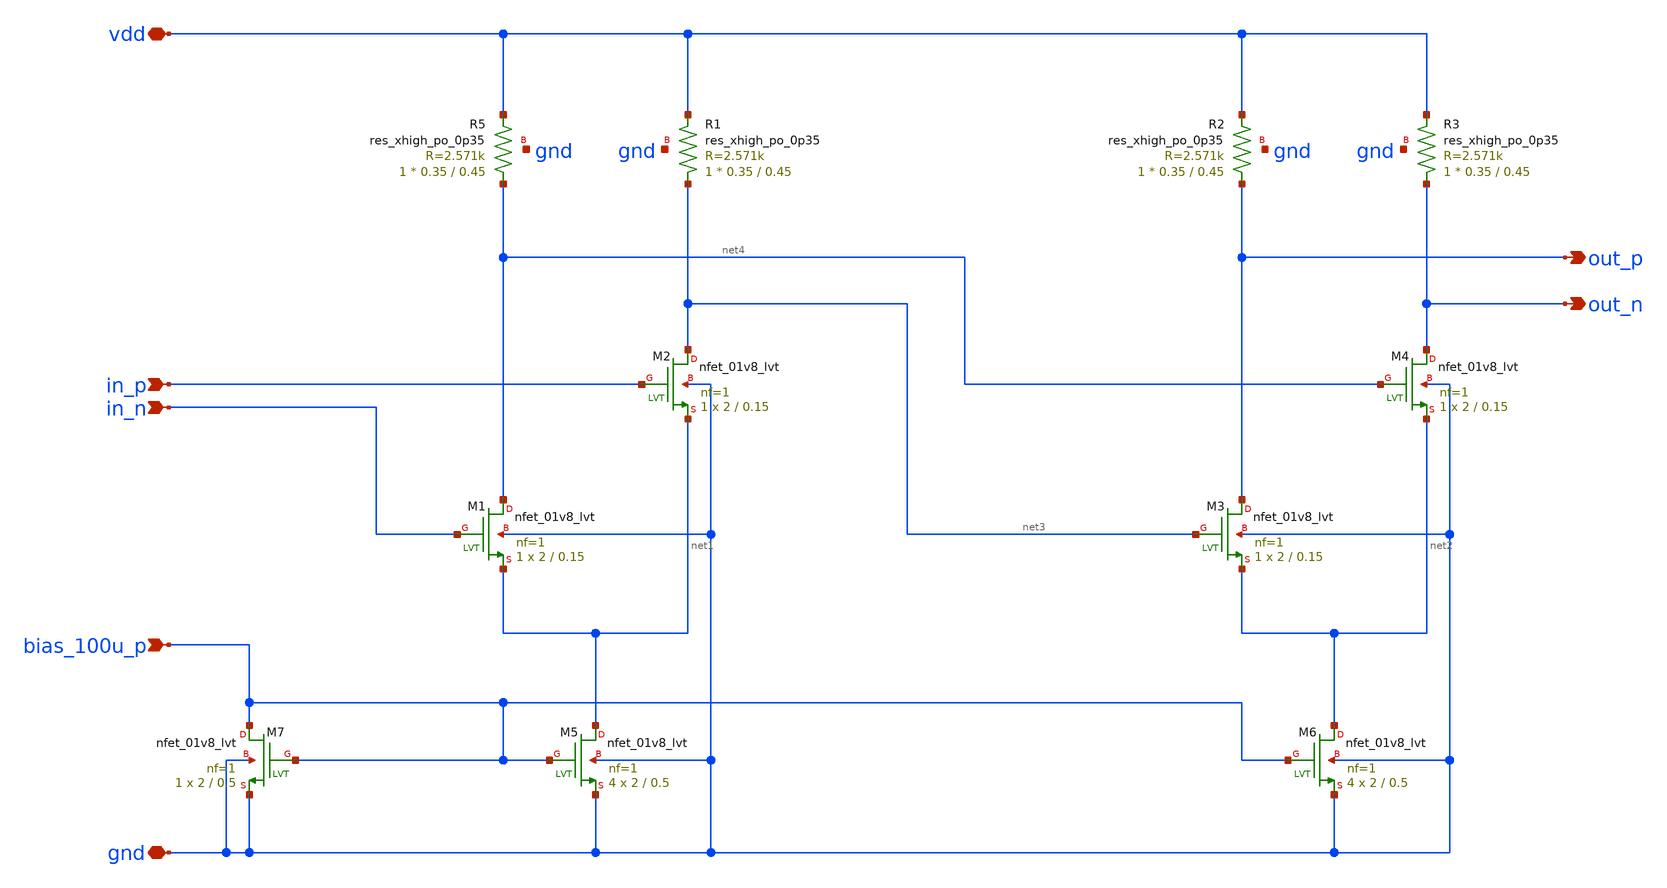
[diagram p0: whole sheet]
** sch_path: design/lc_oscillator_buffer/lc_oscillator_buffer.sch
**.subckt lc_oscillator_buffer gnd vdd out_p out_n bias_100u_p in_p in_n
*.iopin gnd
*.iopin vdd
*.opin out_p
*.opin out_n
*.ipin bias_100u_p
*.ipin in_p
*.ipin in_n
XM1 net4 in_n net1 gnd sky130_fd_pr__nfet_01v8_lvt L=0.15 W=2 nf=1 ad='int((nf+1)/2) * W/nf * 0.29' as='int((nf+2)/2) * W/nf * 0.29'
+ pd='2*int((nf+1)/2) * (W/nf + 0.29)' ps='2*int((nf+2)/2) * (W/nf + 0.29)' nrd='0.29 / W' nrs='0.29 / W'
+ sa=0 sb=0 sd=0 mult=1 m=1
XM2 net3 in_p net1 gnd sky130_fd_pr__nfet_01v8_lvt L=0.15 W=2 nf=1 ad='int((nf+1)/2) * W/nf * 0.29' as='int((nf+2)/2) * W/nf * 0.29'
+ pd='2*int((nf+1)/2) * (W/nf + 0.29)' ps='2*int((nf+2)/2) * (W/nf + 0.29)' nrd='0.29 / W' nrs='0.29 / W'
+ sa=0 sb=0 sd=0 mult=1 m=1
XM3 out_p net3 net2 gnd sky130_fd_pr__nfet_01v8_lvt L=0.15 W=2 nf=1 ad='int((nf+1)/2) * W/nf * 0.29'
+ as='int((nf+2)/2) * W/nf * 0.29' pd='2*int((nf+1)/2) * (W/nf + 0.29)' ps='2*int((nf+2)/2) * (W/nf + 0.29)'
+ nrd='0.29 / W' nrs='0.29 / W' sa=0 sb=0 sd=0 mult=1 m=1
XM4 out_n net4 net2 gnd sky130_fd_pr__nfet_01v8_lvt L=0.15 W=2 nf=1 ad='int((nf+1)/2) * W/nf * 0.29'
+ as='int((nf+2)/2) * W/nf * 0.29' pd='2*int((nf+1)/2) * (W/nf + 0.29)' ps='2*int((nf+2)/2) * (W/nf + 0.29)'
+ nrd='0.29 / W' nrs='0.29 / W' sa=0 sb=0 sd=0 mult=1 m=1
XR5 net4 vdd gnd sky130_fd_pr__res_xhigh_po_0p35 L=0.45 mult=1 m=1
XR1 net3 vdd gnd sky130_fd_pr__res_xhigh_po_0p35 L=0.45 mult=1 m=1
XM5 net1 bias_100u_p gnd gnd sky130_fd_pr__nfet_01v8_lvt L=0.5 W=2 nf=1 ad='int((nf+1)/2) * W/nf * 0.29'
+ as='int((nf+2)/2) * W/nf * 0.29' pd='2*int((nf+1)/2) * (W/nf + 0.29)' ps='2*int((nf+2)/2) * (W/nf + 0.29)'
+ nrd='0.29 / W' nrs='0.29 / W' sa=0 sb=0 sd=0 mult=4 m=4
XM6 net2 bias_100u_p gnd gnd sky130_fd_pr__nfet_01v8_lvt L=0.5 W=2 nf=1 ad='int((nf+1)/2) * W/nf * 0.29'
+ as='int((nf+2)/2) * W/nf * 0.29' pd='2*int((nf+1)/2) * (W/nf + 0.29)' ps='2*int((nf+2)/2) * (W/nf + 0.29)'
+ nrd='0.29 / W' nrs='0.29 / W' sa=0 sb=0 sd=0 mult=4 m=4
XM7 bias_100u_p bias_100u_p gnd gnd sky130_fd_pr__nfet_01v8_lvt L=0.5 W=2 nf=1 ad='int((nf+1)/2) * W/nf * 0.29'
+ as='int((nf+2)/2) * W/nf * 0.29' pd='2*int((nf+1)/2) * (W/nf + 0.29)' ps='2*int((nf+2)/2) * (W/nf + 0.29)'
+ nrd='0.29 / W' nrs='0.29 / W' sa=0 sb=0 sd=0 mult=1 m=1
XR2 out_p vdd gnd sky130_fd_pr__res_xhigh_po_0p35 L=0.45 mult=1 m=1
XR3 out_n vdd gnd sky130_fd_pr__res_xhigh_po_0p35 L=0.45 mult=1 m=1
**.ends
.end
